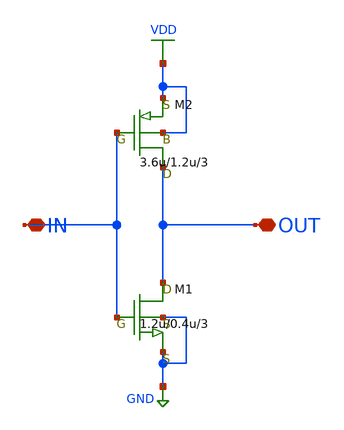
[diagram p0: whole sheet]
** sch_path: LR_hasegawa/LR_Work2/Citizen035/INVERTER3_Citizen.sch
**.subckt INVERTER3_Citizen OUT IN
*.iopin OUT
*.iopin IN
M1 OUT IN GND GND nch w=1.2u l=0.4u as=0 ps=0 ad=0 pd=0 m=3
M2 OUT IN VDD VDD pch w=3.6u l=1.2u as=0 ps=0 ad=0 pd=0 m=3
**.ends
.GLOBAL VDD
.GLOBAL GND
.end
